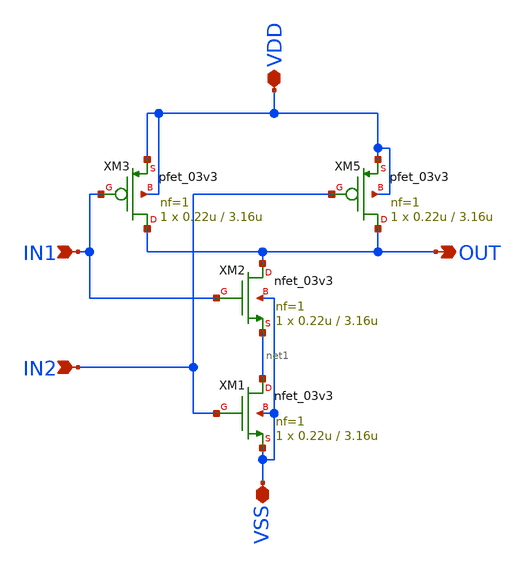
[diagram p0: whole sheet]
** sch_path: designs/DS_modulator/clkgen_nand/xscheme/clkgen_nand.sch
**.subckt clkgen_nand IN1 OUT VDD IN2 VSS
*.ipin IN1
*.opin OUT
*.iopin VDD
*.ipin IN2
*.iopin VSS
XM1 net1 IN2 VSS VSS nfet_03v3 L=3.16u W=0.22u nf=1 ad='int((nf+1)/2) * W/nf * 0.18u' as='int((nf+2)/2) * W/nf * 0.18u'
+ pd='2*int((nf+1)/2) * (W/nf + 0.18u)' ps='2*int((nf+2)/2) * (W/nf + 0.18u)' nrd='0.18u / W' nrs='0.18u / W'
+ sa=0 sb=0 sd=0 m=1
XM2 OUT IN1 net1 VSS nfet_03v3 L=3.16u W=0.22u nf=1 ad='int((nf+1)/2) * W/nf * 0.18u' as='int((nf+2)/2) * W/nf * 0.18u'
+ pd='2*int((nf+1)/2) * (W/nf + 0.18u)' ps='2*int((nf+2)/2) * (W/nf + 0.18u)' nrd='0.18u / W' nrs='0.18u / W'
+ sa=0 sb=0 sd=0 m=1
XM3 OUT IN1 VDD VDD pfet_03v3 L=3.16u W=0.22u nf=1 ad='int((nf+1)/2) * W/nf * 0.18u' as='int((nf+2)/2) * W/nf * 0.18u'
+ pd='2*int((nf+1)/2) * (W/nf + 0.18u)' ps='2*int((nf+2)/2) * (W/nf + 0.18u)' nrd='0.18u / W' nrs='0.18u / W'
+ sa=0 sb=0 sd=0 m=1
XM5 OUT IN2 VDD VDD pfet_03v3 L=3.16u W=0.22u nf=1 ad='int((nf+1)/2) * W/nf * 0.18u' as='int((nf+2)/2) * W/nf * 0.18u'
+ pd='2*int((nf+1)/2) * (W/nf + 0.18u)' ps='2*int((nf+2)/2) * (W/nf + 0.18u)' nrd='0.18u / W' nrs='0.18u / W'
+ sa=0 sb=0 sd=0 m=1
**.ends
.end
